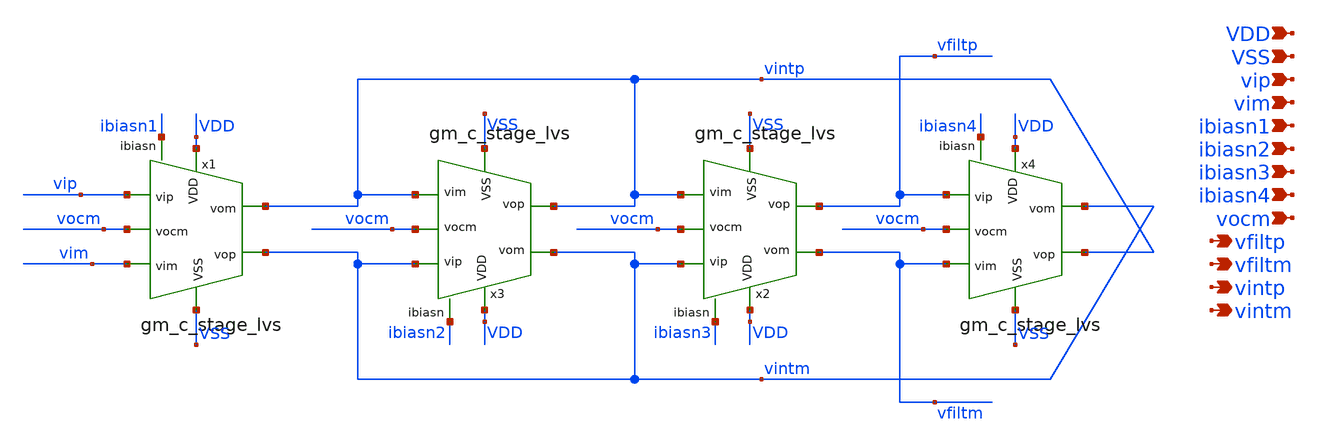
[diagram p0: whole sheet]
** sch_path: designs/biquad_gm_c_filter_lvs.sch
* Copyright 2020 Stefan Frederik Schippers
* Licensed under the Apache License, Version 2.0 (the "License");
* you may not use this file except in compliance with the License.
* You may obtain a copy of the License at
* https://www.apache.org/licenses/LICENSE-2.0
* Unless required by applicable law or agreed to in writing, software
* distributed under the License is distributed on an "AS IS" BASIS,
* WITHOUT WARRANTIES OR CONDITIONS OF ANY KIND, either express or implied.
* See the License for the specific language governing permissions and
* limitations under the License.
**.subckt biquad_gm_c_filter_lvs VDD VSS vip vim ibiasn1 vocm vfiltp vfiltm vintp vintm ibiasn2
*+ ibiasn3 ibiasn4
*.ipin VDD
*.ipin VSS
*.ipin vip
*.ipin vim
*.ipin ibiasn1
*.ipin vocm
*.opin vfiltp
*.opin vfiltm
*.opin vintp
*.opin vintm
*.ipin ibiasn2
*.ipin ibiasn3
*.ipin ibiasn4
x1 vintp vintm vip vim vocm VDD VSS ibiasn1 gm_c_stage_lvs Itail=0.01u Wp=0.5 Wn_diff=8 Wpcm=0.5
+ Wncm=8 Wn_bias=1 Lp=1 Ln_diff=1 Lpcm=1 Lncm=1 Ln_bias=4
x4 vintm vintp vfiltp vfiltm vocm VDD VSS ibiasn4 gm_c_stage_lvs Itail=0.01u Wp=0.5 Wn_diff=8
+ Wpcm=0.5 Wncm=8 Wn_bias=1 Lp=1 Ln_diff=1 Lpcm=1 Lncm=1 Ln_bias=4
x2 vfiltm vfiltp vintm vintp vocm VDD VSS ibiasn3 gm_c_stage_lvs Itail=0.01u Wp=0.5 Wn_diff=8
+ Wpcm=0.5 Wncm=8 Wn_bias=1 Lp=1 Ln_diff=1 Lpcm=1 Lncm=1 Ln_bias=4
x3 vintm vintp vintm vintp vocm VDD VSS ibiasn2 gm_c_stage_lvs Itail=0.01u Wp=0.5 Wn_diff=8 Wpcm=0.5
+ Wncm=8 Wn_bias=1 Lp=1 Ln_diff=1 Lpcm=1 Lncm=1 Ln_bias=4
**.ends
.end
